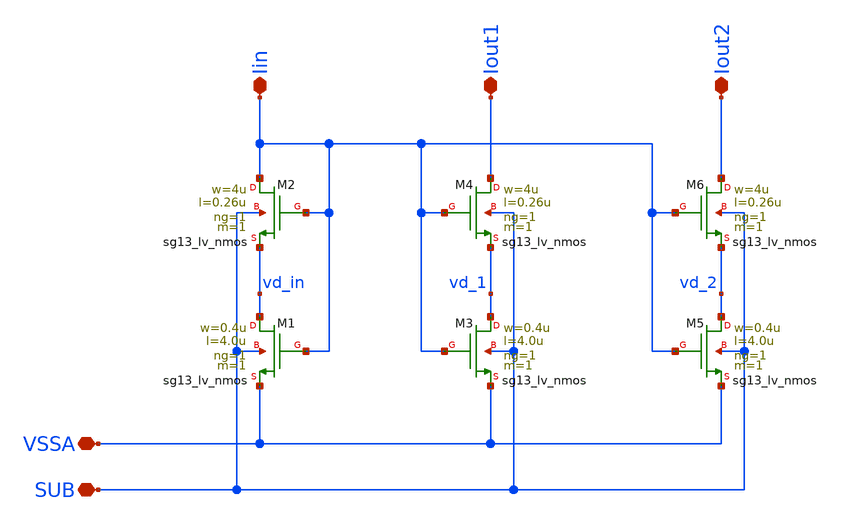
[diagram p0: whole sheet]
** sch_path: xschem/Nmirror.sch
**.subckt Nmirror VSSA SUB Iin Iout1 Iout2
*.iopin VSSA
*.iopin SUB
*.iopin Iin
*.iopin Iout1
*.iopin Iout2
XM1 vd_in Iin VSSA SUB sg13_lv_nmos w=0.4u l=4.0u ng=1 m=1 mm_ok=1
XM3 vd_1 Iin VSSA SUB sg13_lv_nmos w=0.4u l=4.0u ng=1 m=1 mm_ok=1
XM2 Iin Iin vd_in SUB sg13_lv_nmos w=4u l=0.26u ng=1 m=1 mm_ok=1
XM4 Iout1 Iin vd_1 SUB sg13_lv_nmos w=4u l=0.26u ng=1 m=1 mm_ok=1
XM5 vd_2 Iin VSSA SUB sg13_lv_nmos w=0.4u l=4.0u ng=1 m=1 mm_ok=1
XM6 Iout2 Iin vd_2 SUB sg13_lv_nmos w=4u l=0.26u ng=1 m=1 mm_ok=1
**.ends
.end
